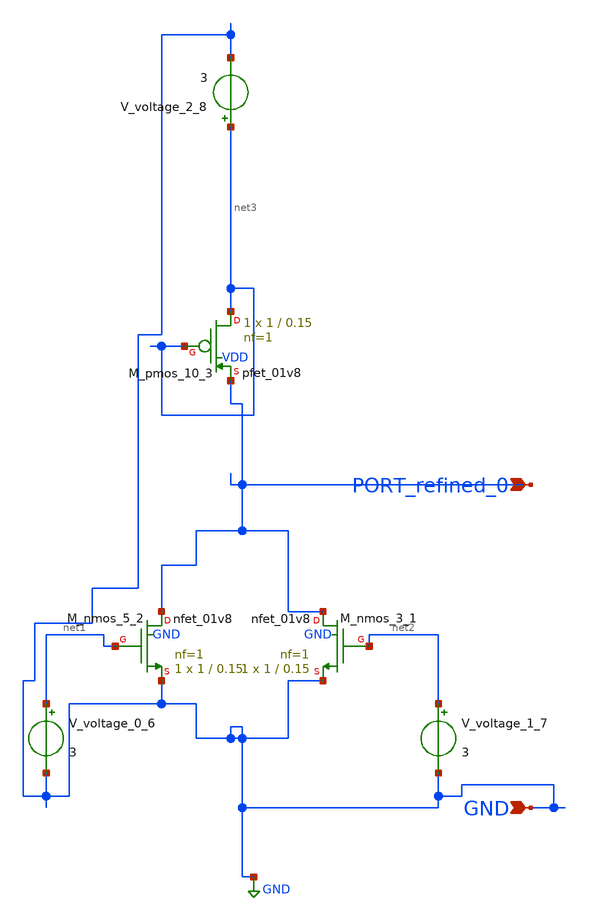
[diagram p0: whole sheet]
** sch_path: schematics/10_1007_s12274-008-8033-4_09_001.sch
**.subckt 10_1007_s12274-008-8033-4_09_001 PORT_refined_0 GND
*.ipin PORT_refined_0
*.ipin GND
XM_nmos_3_1 PORT_refined_0 net2 GND GND sky130_fd_pr__nfet_01v8 L=0.15 W=1 nf=1 ad='int((1 + 1)/2) * 1 / 1 * 0.29'
+ as='int((1 + 2)/2) * 1 / 1 * 0.29' pd='2*int((1 + 1)/2) * (1 / 1 + 0.29)' ps='2*int((1 + 2)/2) * (1 / 1 + 0.29)'
+ nrd='0.29 / 1 ' nrs='0.29 / 1 ' sa=0 sb=0 sd=0 mult=1 m=1
XM_nmos_5_2 PORT_refined_0 net1 GND GND sky130_fd_pr__nfet_01v8 L=0.15 W=1 nf=1 ad='int((1 + 1)/2) * 1 / 1 * 0.29'
+ as='int((1 + 2)/2) * 1 / 1 * 0.29' pd='2*int((1 + 1)/2) * (1 / 1 + 0.29)' ps='2*int((1 + 2)/2) * (1 / 1 + 0.29)'
+ nrd='0.29 / 1 ' nrs='0.29 / 1 ' sa=0 sb=0 sd=0 mult=1 m=1
XM_pmos_10_3 net3 net3 PORT_refined_0 VDD sky130_fd_pr__pfet_01v8 L=0.15 W=1 nf=1 ad='int((1 + 1)/2) * 1 / 1 * 0.29'
+ as='int((1 + 2)/2) * 1 / 1 * 0.29' pd='2*int((1 + 1)/2) * (1 / 1 + 0.29)' ps='2*int((1 + 2)/2) * (1 / 1 + 0.29)'
+ nrd='0.29 / 1 ' nrs='0.29 / 1 ' sa=0 sb=0 sd=0 mult=1 m=1
V_voltage_0_6 net1 GND 3
V_voltage_1_7 net2 GND 3
V_voltage_2_8 net3 GND 3
**.ends
.GLOBAL GND
.end
